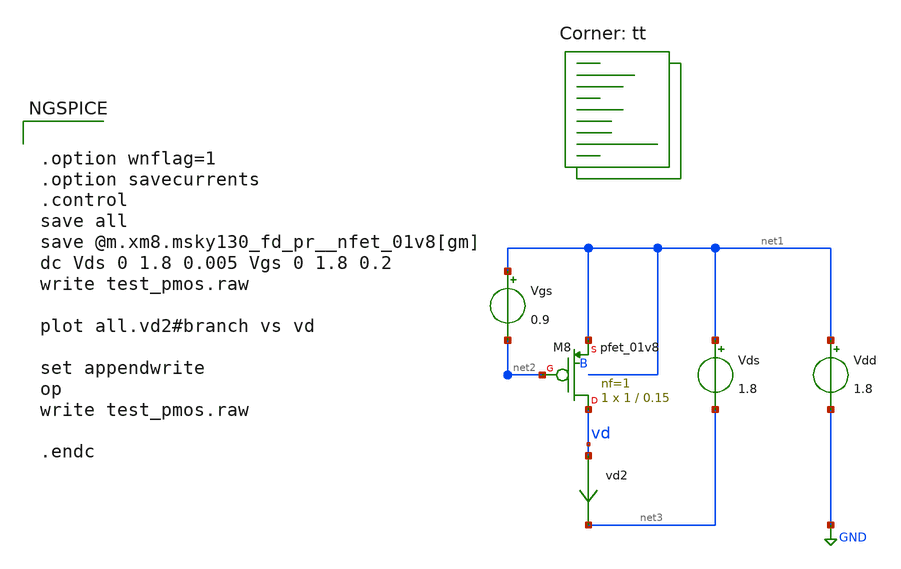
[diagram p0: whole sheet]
** sch_path: Modulo_Analogico/Lab1/dc_pfet_01v8.sch
**.subckt dc_pfet_01v8
Vgs net1 net2 0.9
Vds net1 net3 1.8
vd2 vd net3 0
.save i(vd2)
Vdd net1 GND 1.8
XM8 vd net2 net1 B sky130_fd_pr__pfet_01v8 L=0.15 W=1 nf=1 ad='int((1 + 1)/2) * 1 / 1 * 0.29' as='int((1 + 2)/2) * 1 / 1 * 0.29'
+ pd='2*int((1 + 1)/2) * (1 / 1 + 0.29)' ps='2*int((1 + 2)/2) * (1 / 1 + 0.29)' nrd='0.29 / 1 ' nrs='0.29 / 1 '
+ sa=0 sb=0 sd=0 mult=1 m=1
**** begin user architecture code
.lib $::SKYWATER_MODELS/sky130.lib.spice tt


.option wnflag=1
.option savecurrents
.control
save all
save @m.xm8.msky130_fd_pr__nfet_01v8[gm]
dc Vds 0 1.8 0.005 Vgs 0 1.8 0.2
write test_pmos.raw

plot all.vd2#branch vs vd

set appendwrite
op
write test_pmos.raw

.endc


**** end user architecture code
**.ends
.GLOBAL GND
.end
